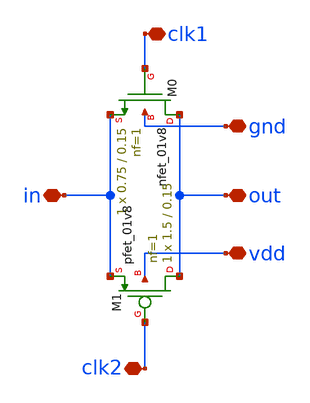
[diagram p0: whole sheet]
** sch_path: sch/simulation/passGate/passGate.sch
**.subckt passGate out in clk1 clk2 gnd vdd
*.iopin out
*.iopin in
*.iopin clk1
*.iopin clk2
*.iopin gnd
*.iopin vdd
XM0 out clk1 in gnd sky130_fd_pr__nfet_01v8 L=0.15 W=0.75 nf=1 ad='int((nf+1)/2) * W/nf * 0.29' as='int((nf+2)/2) * W/nf * 0.29'
+ pd='2*int((nf+1)/2) * (W/nf + 0.29)' ps='2*int((nf+2)/2) * (W/nf + 0.29)' nrd='0.29 / W' nrs='0.29 / W'
+ sa=0 sb=0 sd=0 mult=1 m=1
XM1 out clk2 in vdd sky130_fd_pr__pfet_01v8 L=0.15 W=1.5 nf=1 ad='int((nf+1)/2) * W/nf * 0.29' as='int((nf+2)/2) * W/nf * 0.29'
+ pd='2*int((nf+1)/2) * (W/nf + 0.29)' ps='2*int((nf+2)/2) * (W/nf + 0.29)' nrd='0.29 / W' nrs='0.29 / W'
+ sa=0 sb=0 sd=0 mult=1 m=1
**.ends
.end
